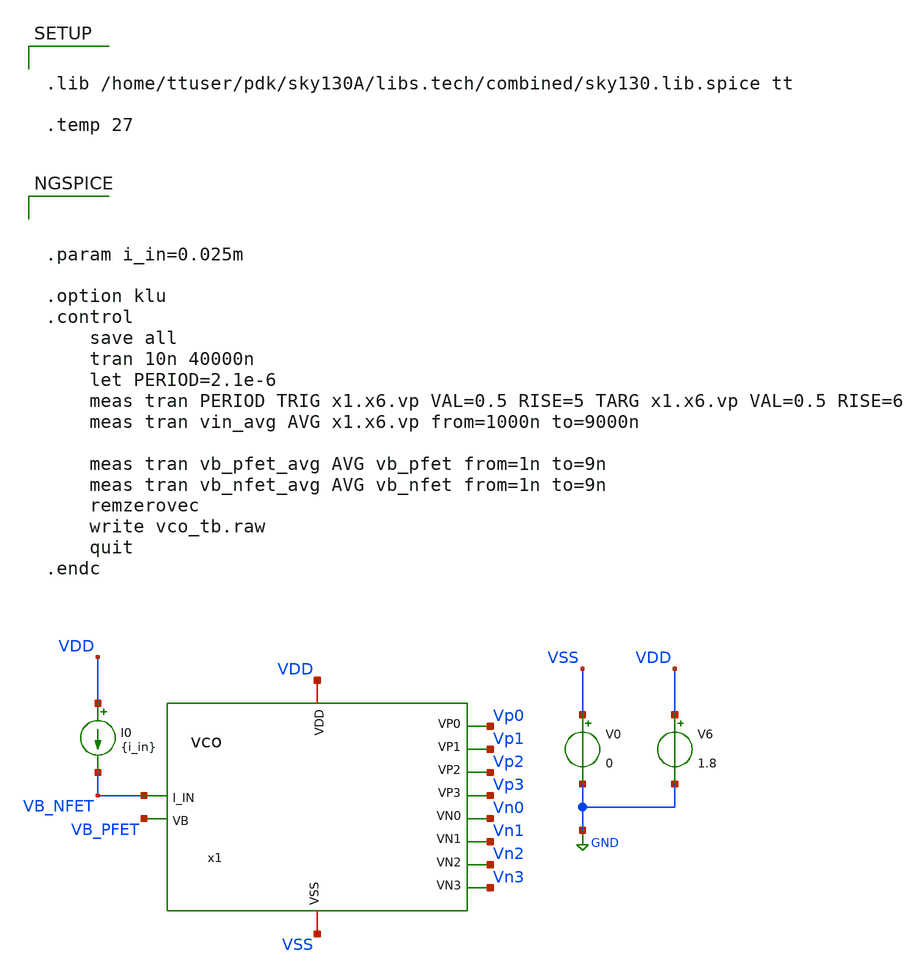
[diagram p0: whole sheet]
** sch_path: xschem/vco_tb.sch
**.subckt vco_tb
V0 VSS GND 0
V6 VDD GND 1.8
I0 VDD VB_NFET {i_in}
x1 VDD VSS VB_NFET Vp0 Vp1 Vp2 Vp3 Vn0 Vn1 Vn2 Vn3 VB_PFET vco
**** begin user architecture code



.param i_in=0.025m

.option klu
.control
	save all
	tran 10n 40000n
	let PERIOD=2.1e-6
	meas tran PERIOD TRIG x1.x6.vp VAL=0.5 RISE=5 TARG x1.x6.vp VAL=0.5 RISE=6
	meas tran vin_avg AVG x1.x6.vp from=1000n to=9000n

	meas tran vb_pfet_avg AVG vb_pfet from=1n to=9n
	meas tran vb_nfet_avg AVG vb_nfet from=1n to=9n
	remzerovec
	write vco_tb.raw
	quit
.endc




.lib /home/ttuser/pdk/sky130A/libs.tech/combined/sky130.lib.spice tt

.temp 27


**** end user architecture code
**.ends
.GLOBAL GND
.end
